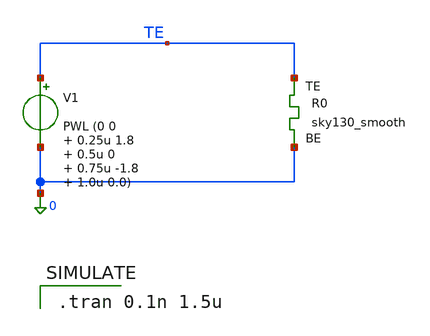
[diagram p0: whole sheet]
** sch_path: memristor_models/sky130_smooth/tb_sky130_smooth.sch
**.subckt tb_sky130_smooth
V1 TE 0 PWL (0 0 0.25u 1.8 0.5u 0 0.75u -1.8 1.0u 0.0)
XR0 TE 0 sky130_smooth Tfilament_0=3.8e-9
**** begin user architecture code

.tran 0.1n 1.5u


** opencircuitdesign pdks install
.inc $::SKYWATER_MODELS/sky130_smooth.spice


.control
save all
run
write tb_sky130_smooth.raw
.endc



**** end user architecture code
**.ends
.end
